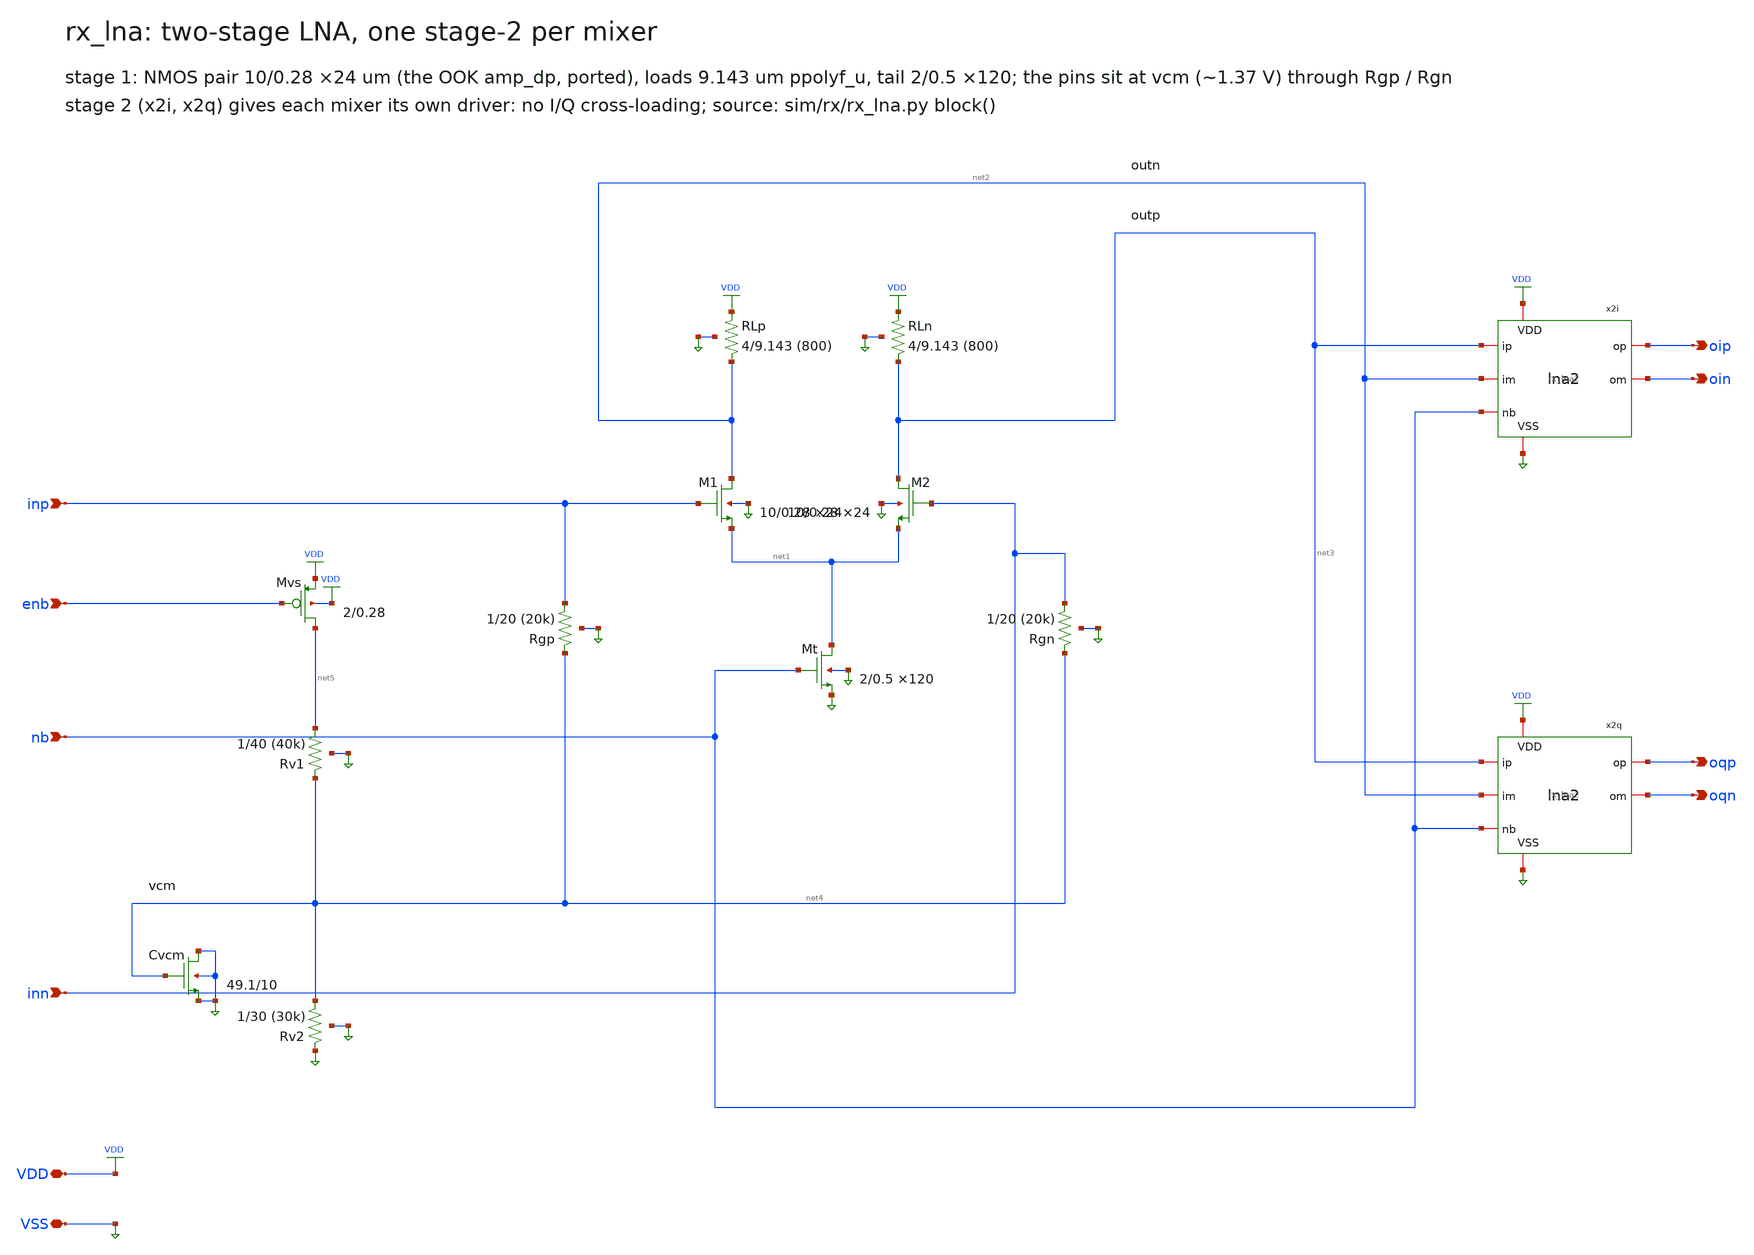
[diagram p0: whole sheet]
** sch_path: xschem/rx_lna.sch
**.subckt rx_lna VDD VSS inp inn oip oin oqp oqn nb enb
*.iopin VDD
*.iopin VSS
*.ipin inp
*.ipin inn
*.opin oip
*.opin oin
*.opin oqp
*.opin oqn
*.ipin nb
*.ipin enb
XM1 net2 inp net1 VSS nfet_03v3 L=0.28u W=10.0u nf=1 ad=5.0p as=5.0p pd=21.0u ps=21.0u nrd=0 nrs=0
+ sa=0 sb=0 sd=0 m=24
XM2 net3 inn net1 VSS nfet_03v3 L=0.28u W=10.0u nf=1 ad=5.0p as=5.0p pd=21.0u ps=21.0u nrd=0 nrs=0
+ sa=0 sb=0 sd=0 m=24
XMt net1 nb VSS VSS nfet_03v3 L=0.5u W=2.0u nf=1 ad=1.0p as=1.0p pd=5.0u ps=5.0u nrd=0 nrs=0 sa=0
+ sb=0 sd=0 m=120
XRLp net2 VDD VSS ppolyf_u r_width=4.0e-6 r_length=9.143e-6 m=1
XRLn net3 VDD VSS ppolyf_u r_width=4.0e-6 r_length=9.143e-6 m=1
XRgp inp net4 VSS ppolyf_u_1k r_width=1.0e-6 r_length=20.0e-6 m=1
XRgn inn net4 VSS ppolyf_u_1k r_width=1.0e-6 r_length=20.0e-6 m=1
XMvs net5 enb VDD VDD pfet_03v3 L=0.28u W=2.0u nf=1 ad=1.0p as=1.0p pd=5.0u ps=5.0u nrd=0 nrs=0 sa=0
+ sb=0 sd=0 m=1
XRv1 net5 net4 VSS ppolyf_u_1k r_width=1.0e-6 r_length=40.0e-6 m=1
XRv2 net4 VSS VSS ppolyf_u_1k r_width=1.0e-6 r_length=30.0e-6 m=1
XCvcm VSS net4 VSS VSS nfet_03v3 L=10.0u W=49.14u nf=1 ad=24.57p as=24.57p pd=99.28u ps=99.28u nrd=0
+ nrs=0 sa=0 sb=0 sd=0 m=1
x2i VDD VSS net3 net2 oip oin nb rx_lna2
x2q VDD VSS net3 net2 oqp oqn nb rx_lna2
**.ends

* expanding   symbol:  rx_lna2.sym # of pins=7
** sym_path: xschem/rx_lna2.sym
** sch_path: xschem/rx_lna2.sch
.subckt rx_lna2 VDD VSS ip im op om nb
*.iopin VDD
*.iopin VSS
*.ipin ip
*.ipin im
*.opin op
*.opin om
*.ipin nb
XM1 om ip net1 VSS nfet_03v3 L=0.28u W=10.0u nf=1 ad=5.0p as=5.0p pd=21.0u ps=21.0u nrd=0 nrs=0 sa=0
+ sb=0 sd=0 m=6
XM2 op im net1 VSS nfet_03v3 L=0.28u W=10.0u nf=1 ad=5.0p as=5.0p pd=21.0u ps=21.0u nrd=0 nrs=0 sa=0
+ sb=0 sd=0 m=6
XMt net1 nb VSS VSS nfet_03v3 L=0.5u W=2.0u nf=1 ad=1.0p as=1.0p pd=5.0u ps=5.0u nrd=0 nrs=0 sa=0
+ sb=0 sd=0 m=40
XRLp om VDD VSS ppolyf_u r_width=2.0e-6 r_length=9.143e-6 m=1
XRLn op VDD VSS ppolyf_u r_width=2.0e-6 r_length=9.143e-6 m=1
.ends

.end
